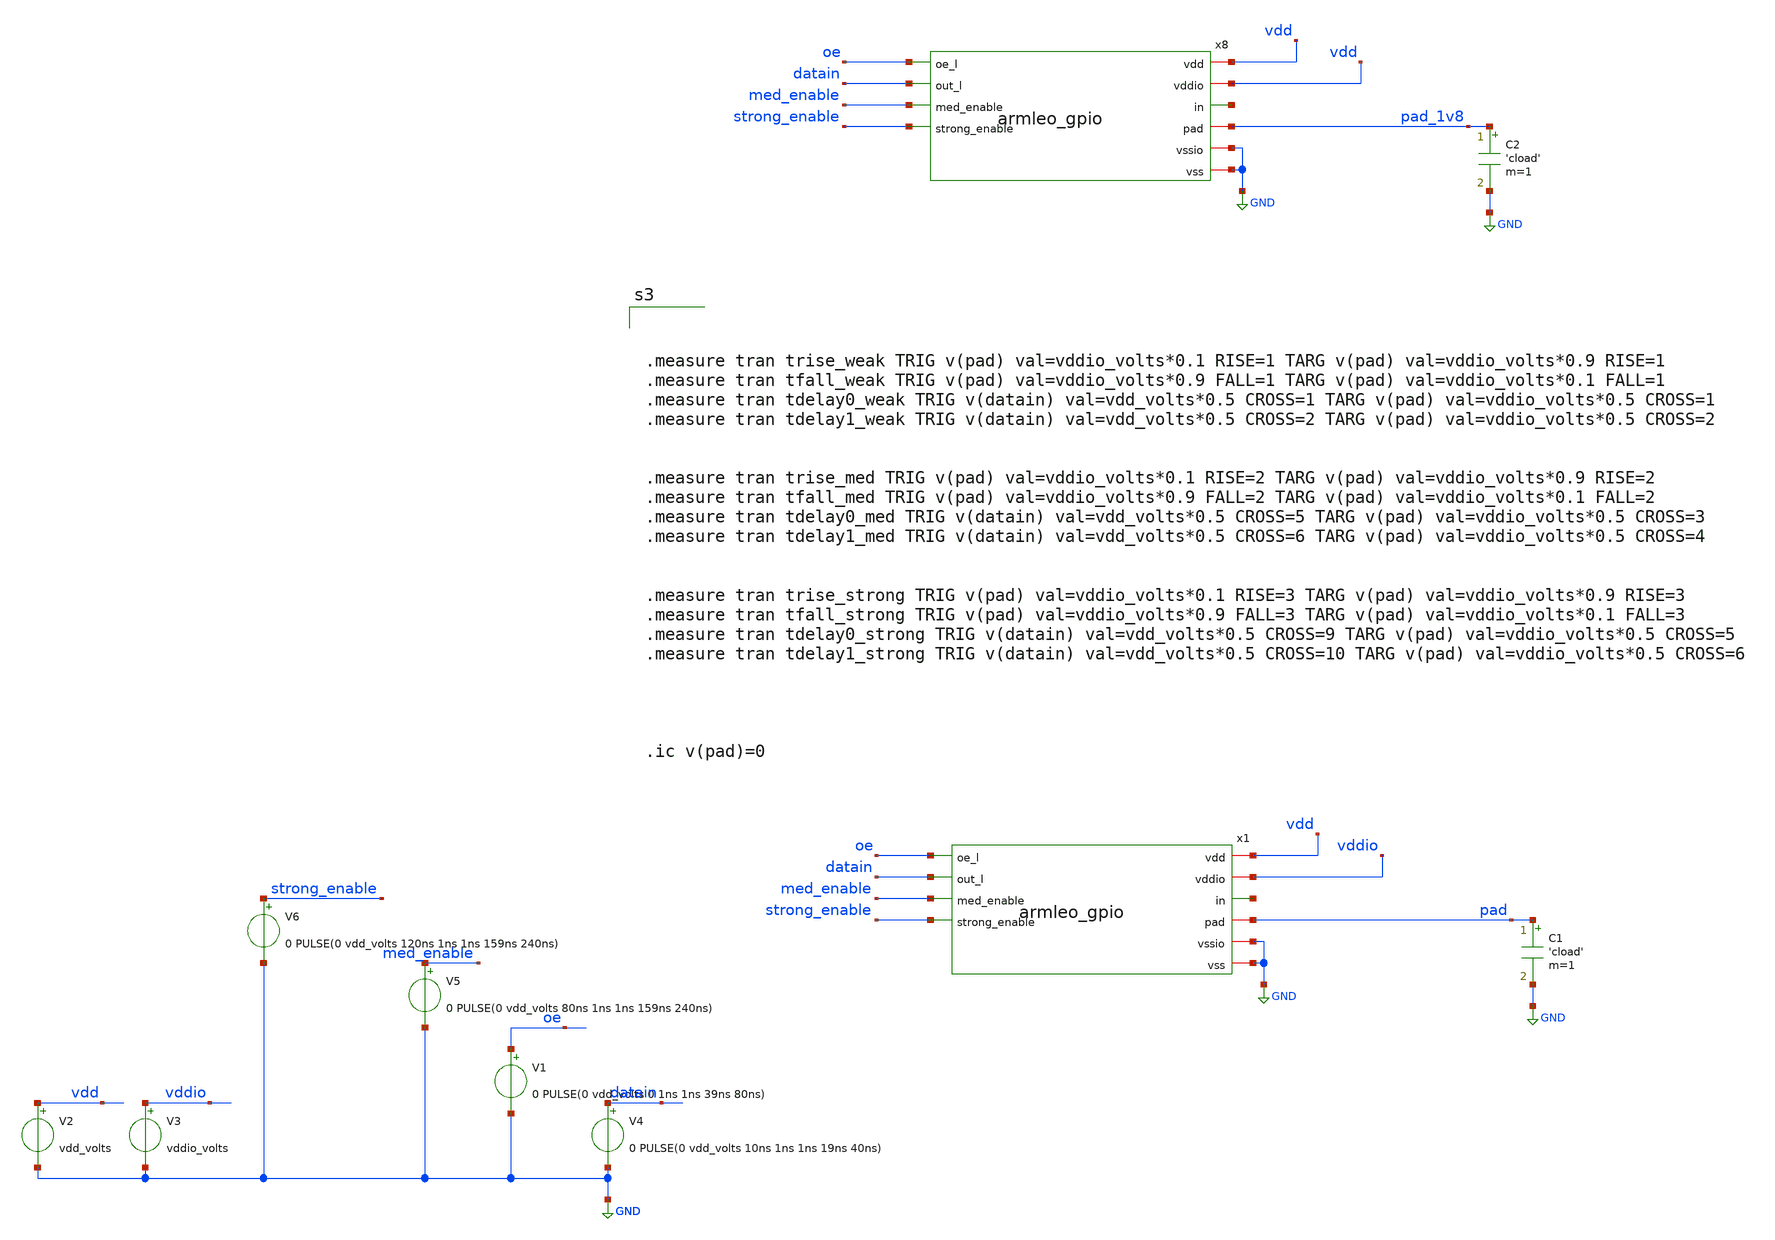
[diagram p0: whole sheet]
** sch_path: xschem/gpio/testbenches/armleo_gpio_worst_tb.sch
**.subckt armleo_gpio_worst_tb
V1 oe GND 0 PULSE(0 vdd_volts 0 1ns 1ns 39ns 80ns)
V2 vdd GND vdd_volts
C1 pad GND 'cload' m=1
V3 vddio GND vddio_volts
x1 vdd vddio net1 pad oe datain med_enable strong_enable GND GND armleo_gpio
V4 datain GND 0 PULSE(0 vdd_volts 10ns 1ns 1ns 19ns 40ns)
x8 vdd vdd net2 pad_1v8 oe datain med_enable strong_enable GND GND armleo_gpio
C2 pad_1v8 GND 'cload' m=1
V5 med_enable GND 0 PULSE(0 vdd_volts 80ns 1ns 1ns 159ns 240ns)
V6 strong_enable GND 0 PULSE(0 vdd_volts 120ns 1ns 1ns 159ns 240ns)
**** begin user architecture code



*.temp -40

*.lib "/opt/pdk_root/sky130A/libs.tech/ngspice/sky130.lib.spice" ff

*.param vdd_volts=1.95
*.param vddio_volts=3.6


.temp 125

.lib "/opt/pdk_root/sky130A/libs.tech/ngspice/sky130.lib.spice" ss

.param vdd_volts=1.65
.param vddio_volts=3.0


.param cload=6pf
*.param cload=12pf


.control
tran 500ps 240ns
write gpio/results/armleo_gpio_tb_6pf_worst.raw

echo "Starting 12pf test"

alterparam cload=12pf
reset
tran 500ps 240ns
write gpio/results/armleo_gpio_tb_12pf_worst.raw


exit
.endc

.param mc_mm_switch=0

*.include "/opt/pdk_root/sky130A/libs.ref/sky130_fd_io/spice/sky130_fd_io.spice"
*.include "/opt/pdk_root/sky130A/libs.ref/sky130_fd_sc_hd/spice/sky130_fd_sc_hd.spice"
*.include "/opt/pdk_root/sky130A/libs.ref/sky130_fd_sc_hvl/spice/sky130_fd_sc_hvl.spice"

.include "libs.spice"






.measure tran trise_weak_1v8 TRIG v(pad_1v8) val=vdd_volts*0.1 RISE=1 TARG v(pad_1v8)
+ val=vdd_volts*0.9 RISE=1
.measure tran tfall_weak_1v8 TRIG v(pad_1v8) val=vdd_volts*0.9 FALL=1 TARG v(pad_1v8)
+ val=vdd_volts*0.1 FALL=1
.measure tran tdelay0_weak_1v8 TRIG v(datain) val=vdd_volts*0.5 CROSS=1 TARG v(pad_1v8)
+ val=vdd_volts*0.5 CROSS=1
.measure tran tdelay1_weak_1v8 TRIG v(datain) val=vdd_volts*0.5 CROSS=2 TARG v(pad_1v8)
+ val=vdd_volts*0.5 CROSS=2

.measure tran trise_med_1v8 TRIG v(pad_1v8) val=vdd_volts*0.1 RISE=2 TARG v(pad_1v8)
+ val=vdd_volts*0.9 RISE=2
.measure tran tfall_med_1v8 TRIG v(pad_1v8) val=vdd_volts*0.9 FALL=2 TARG v(pad_1v8)
+ val=vdd_volts*0.1 FALL=2
.measure tran tdelay0_med_1v8 TRIG v(datain) val=vdd_volts*0.5 CROSS=5 TARG v(pad_1v8)
+ val=vdd_volts*0.5 CROSS=3
.measure tran tdelay1_med_1v8 TRIG v(datain) val=vdd_volts*0.5 CROSS=6 TARG v(pad_1v8)
+ val=vdd_volts*0.5 CROSS=4


.measure tran trise_strong_1v8 TRIG v(pad_1v8) val=vdd_volts*0.1 RISE=3 TARG v(pad_1v8)
+ val=vdd_volts*0.9 RISE=3
.measure tran tfall_strong_1v8 TRIG v(pad_1v8) val=vdd_volts*0.9 FALL=3 TARG v(pad_1v8)
+ val=vdd_volts*0.1 FALL=3
.measure tran tdelay0_strong_1v8 TRIG v(datain) val=vdd_volts*0.5 CROSS=9 TARG v(pad_1v8)
+ val=vdd_volts*0.5 CROSS=5
.measure tran tdelay1_strong_1v8 TRIG v(datain) val=vdd_volts*0.5 CROSS=10 TARG v(pad_1v8)
+ val=vdd_volts*0.5 CROSS=6



.ic v(pad_1v8)=0





.measure tran trise_weak TRIG v(pad) val=vddio_volts*0.1 RISE=1 TARG v(pad) val=vddio_volts*0.9
+ RISE=1
.measure tran tfall_weak TRIG v(pad) val=vddio_volts*0.9 FALL=1 TARG v(pad) val=vddio_volts*0.1
+ FALL=1
.measure tran tdelay0_weak TRIG v(datain) val=vdd_volts*0.5 CROSS=1 TARG v(pad) val=vddio_volts*0.5
+ CROSS=1
.measure tran tdelay1_weak TRIG v(datain) val=vdd_volts*0.5 CROSS=2 TARG v(pad) val=vddio_volts*0.5
+ CROSS=2


.measure tran trise_med TRIG v(pad) val=vddio_volts*0.1 RISE=2 TARG v(pad) val=vddio_volts*0.9
+ RISE=2
.measure tran tfall_med TRIG v(pad) val=vddio_volts*0.9 FALL=2 TARG v(pad) val=vddio_volts*0.1
+ FALL=2
.measure tran tdelay0_med TRIG v(datain) val=vdd_volts*0.5 CROSS=5 TARG v(pad) val=vddio_volts*0.5
+ CROSS=3
.measure tran tdelay1_med TRIG v(datain) val=vdd_volts*0.5 CROSS=6 TARG v(pad) val=vddio_volts*0.5
+ CROSS=4


.measure tran trise_strong TRIG v(pad) val=vddio_volts*0.1 RISE=3 TARG v(pad) val=vddio_volts*0.9
+ RISE=3
.measure tran tfall_strong TRIG v(pad) val=vddio_volts*0.9 FALL=3 TARG v(pad) val=vddio_volts*0.1
+ FALL=3
.measure tran tdelay0_strong TRIG v(datain) val=vdd_volts*0.5 CROSS=9 TARG v(pad)
+ val=vddio_volts*0.5 CROSS=5
.measure tran tdelay1_strong TRIG v(datain) val=vdd_volts*0.5 CROSS=10 TARG v(pad)
+ val=vddio_volts*0.5 CROSS=6




.ic v(pad)=0


**** end user architecture code
**.ends

* expanding   symbol:  gpio/armleo_gpio.sym # of pins=10
** sym_path: xschem/gpio/armleo_gpio.sym
** sch_path: xschem/gpio/armleo_gpio.sch
.subckt armleo_gpio vdd vddio in pad oe_l out_l med_enable strong_enable vssio vss
*.ipin out_l
*.iopin vddio
*.iopin vssio
*.ipin oe_l
*.opin in
*.iopin vdd
*.iopin vss
*.iopin pad
*.ipin med_enable
*.ipin strong_enable
x2 vddio n1 weak_pgate n2 vssio armleo_gpio_lv2hv
x6 esd_pad vss vss vdd vdd in sky130_fd_sc_hvl__buf_16
x37 vddio n3 weak_ngate n4 vssio armleo_gpio_lv2hv
XM1 pad m2_weak_pgate vddio vddio sky130_fd_pr__pfet_g5v0d10v5 L=0.5 W=10 nf=1 ad='int((nf+1)/2) * W/nf * 0.29'
+ as='int((nf+2)/2) * W/nf * 0.29' pd='2*int((nf+1)/2) * (W/nf + 0.29)' ps='2*int((nf+2)/2) * (W/nf + 0.29)'
+ nrd='0.29 / W' nrs='0.29 / W' sa=0 sb=0 sd=0 mult=3*2 m=3*2
XM2 pad m2_weak_ngate vssio vssio sky130_fd_pr__nfet_g5v0d10v5 L=0.5 W=4.5 nf=1 ad='int((nf+1)/2) * W/nf * 0.29'
+ as='int((nf+2)/2) * W/nf * 0.29' pd='2*int((nf+1)/2) * (W/nf + 0.29)' ps='2*int((nf+2)/2) * (W/nf + 0.29)'
+ nrd='0.29 / W' nrs='0.29 / W' sa=0 sb=0 sd=0 mult=3*2 m=3*2
x1 weak_ngate vssio vssio vddio vddio m1_weak_ngate_n sky130_fd_sc_hvl__inv_4
x5 weak_pgate vssio vssio vddio vddio m1_weak_pgate_n sky130_fd_sc_hvl__inv_4
x3 m1_weak_pgate_n vssio vssio vddio vddio m2_weak_pgate sky130_fd_sc_hvl__inv_16
x10 m1_weak_ngate_n vssio vssio vddio vddio m2_weak_ngate sky130_fd_sc_hvl__inv_16
x8 n3 vss vss vdd vdd n4 sky130_fd_sc_hd__inv_4
x12 n1 vss vss vdd vdd n2 sky130_fd_sc_hd__inv_4
x14 oe_l vss vss vdd vdd n5 sky130_fd_sc_hd__inv_4
x16 oe_l out_l vss vss vdd vdd n1 sky130_fd_sc_hd__nand2_4
x17 out_l n5 vss vss vdd vdd n3 sky130_fd_sc_hd__nor2_4
R1 pad esd_pad sky130_fd_pr__res_generic_l1 W=1 L=10 m=1
x4 vddio n1_med med_pgate n2_med vssio armleo_gpio_lv2hv
x7 vddio n3_med med_ngate n4_med vssio armleo_gpio_lv2hv
x9 n3_med vss vss vdd vdd n4_med sky130_fd_sc_hd__inv_4
x11 n1_med vss vss vdd vdd n2_med sky130_fd_sc_hd__inv_4
x13 vddio n1_strong strong_pgate n2_strong vssio armleo_gpio_lv2hv
x15 vddio n3_strong strong_ngate n4_strong vssio armleo_gpio_lv2hv
x18 n3_strong vss vss vdd vdd n4_strong sky130_fd_sc_hd__inv_4
x19 n1_strong vss vss vdd vdd n2_strong sky130_fd_sc_hd__inv_4
XM3 pad m2_med_pgate vddio vddio sky130_fd_pr__pfet_g5v0d10v5 L=0.5 W=10 nf=1 ad='int((nf+1)/2) * W/nf * 0.29'
+ as='int((nf+2)/2) * W/nf * 0.29' pd='2*int((nf+1)/2) * (W/nf + 0.29)' ps='2*int((nf+2)/2) * (W/nf + 0.29)'
+ nrd='0.29 / W' nrs='0.29 / W' sa=0 sb=0 sd=0 mult=3*3 m=3*3
XM4 pad m2_med_ngate vssio vssio sky130_fd_pr__nfet_g5v0d10v5 L=0.5 W=4.5 nf=1 ad='int((nf+1)/2) * W/nf * 0.29'
+ as='int((nf+2)/2) * W/nf * 0.29' pd='2*int((nf+1)/2) * (W/nf + 0.29)' ps='2*int((nf+2)/2) * (W/nf + 0.29)'
+ nrd='0.29 / W' nrs='0.29 / W' sa=0 sb=0 sd=0 mult=3*3 m=3*3
x20 med_ngate vssio vssio vddio vddio m1_med_ngate_n sky130_fd_sc_hvl__inv_4
x21 med_pgate vssio vssio vddio vddio m1_med_pgate_n sky130_fd_sc_hvl__inv_4
x22 m1_med_pgate_n vssio vssio vddio vddio m2_med_pgate sky130_fd_sc_hvl__inv_16
x23 m1_med_ngate_n vssio vssio vddio vddio m2_med_ngate sky130_fd_sc_hvl__inv_16
x24 n6_med vss vss vdd vdd n5_med sky130_fd_sc_hd__inv_4
x25 n5_med out_l vss vss vdd vdd n1_med sky130_fd_sc_hd__nand2_4
x26 out_l n6_med vss vss vdd vdd n3_med sky130_fd_sc_hd__nor2_4
x28 net1 vss vss vdd vdd n5_strong sky130_fd_sc_hd__inv_4
x29 n5_strong out_l vss vss vdd vdd n1_strong sky130_fd_sc_hd__nand2_4
x30 out_l net1 vss vss vdd vdd n3_strong sky130_fd_sc_hd__nor2_4
XM7 pad m2_strong_pgate vddio vddio sky130_fd_pr__pfet_g5v0d10v5 L=0.5 W=10 nf=1 ad='int((nf+1)/2) * W/nf * 0.29'
+ as='int((nf+2)/2) * W/nf * 0.29' pd='2*int((nf+1)/2) * (W/nf + 0.29)' ps='2*int((nf+2)/2) * (W/nf + 0.29)'
+ nrd='0.29 / W' nrs='0.29 / W' sa=0 sb=0 sd=0 mult=3*7 m=3*7
XM8 pad m2_strong_ngate vssio vssio sky130_fd_pr__nfet_g5v0d10v5 L=0.5 W=4.5 nf=1 ad='int((nf+1)/2) * W/nf * 0.29'
+ as='int((nf+2)/2) * W/nf * 0.29' pd='2*int((nf+1)/2) * (W/nf + 0.29)' ps='2*int((nf+2)/2) * (W/nf + 0.29)'
+ nrd='0.29 / W' nrs='0.29 / W' sa=0 sb=0 sd=0 mult=3*7 m=3*7
x36 strong_ngate vssio vssio vddio vddio m1_strong_ngate_n sky130_fd_sc_hvl__inv_4
x38 strong_pgate vssio vssio vddio vddio m1_strong_pgate_n sky130_fd_sc_hvl__inv_4
x39 m1_strong_pgate_n vssio vssio vddio vddio m2_strong_pgate sky130_fd_sc_hvl__inv_16
x40 m1_strong_ngate_n vssio vssio vddio vddio m2_strong_ngate sky130_fd_sc_hvl__inv_16
XM9 pad vssio vssio vssio sky130_fd_pr__esd_nfet_g5v0d10v5 L=0.6 W=5.4 nf=1 ad='int((nf+1)/2) * W/nf * 0.29'
+ as='int((nf+2)/2) * W/nf * 0.29' pd='2*int((nf+1)/2) * (W/nf + 0.29)' ps='2*int((nf+2)/2) * (W/nf + 0.29)'
+ nrd='0.29 / W' nrs='0.29 / W' sa=0 sb=0 sd=0 mult=12 m=12
x27 oe_l med_enable vss vss vdd vdd n6_med sky130_fd_sc_hd__nand2_4
x31 oe_l strong_enable vss vss vdd vdd net1 sky130_fd_sc_hd__nand2_4
.ends


* expanding   symbol:  gpio/armleo_gpio_lv2hv.sym # of pins=5
** sym_path: xschem/gpio/armleo_gpio_lv2hv.sym
** sch_path: xschem/gpio/armleo_gpio_lv2hv.sch
.subckt armleo_gpio_lv2hv VDDH A Y A_N VSSH
*.ipin A
*.iopin VDDH
*.iopin VSSH
*.opin Y
*.ipin A_N
XM2 VSSH A_N Y VSSH sky130_fd_pr__nfet_g5v0d10v5 L=0.5 W=1 nf=1 ad='int((nf+1)/2) * W/nf * 0.29' as='int((nf+2)/2) * W/nf * 0.29'
+ pd='2*int((nf+1)/2) * (W/nf + 0.29)' ps='2*int((nf+2)/2) * (W/nf + 0.29)' nrd='0.29 / W' nrs='0.29 / W'
+ sa=0 sb=0 sd=0 mult=1 m=1
XM5 N1 A VSSH VSSH sky130_fd_pr__nfet_g5v0d10v5 L=0.5 W=1 nf=1 ad='int((nf+1)/2) * W/nf * 0.29' as='int((nf+2)/2) * W/nf * 0.29'
+ pd='2*int((nf+1)/2) * (W/nf + 0.29)' ps='2*int((nf+2)/2) * (W/nf + 0.29)' nrd='0.29 / W' nrs='0.29 / W'
+ sa=0 sb=0 sd=0 mult=1 m=1
XM4 VDDH Y N2 VDDH sky130_fd_pr__pfet_g5v0d10v5 L=0.5 W=1 nf=1 ad='int((nf+1)/2) * W/nf * 0.29' as='int((nf+2)/2) * W/nf * 0.29'
+ pd='2*int((nf+1)/2) * (W/nf + 0.29)' ps='2*int((nf+2)/2) * (W/nf + 0.29)' nrd='0.29 / W' nrs='0.29 / W'
+ sa=0 sb=0 sd=0 mult=1 m=1
XM7 net1 N1 VDDH VDDH sky130_fd_pr__pfet_g5v0d10v5 L=0.5 W=1 nf=1 ad='int((nf+1)/2) * W/nf * 0.29' as='int((nf+2)/2) * W/nf * 0.29'
+ pd='2*int((nf+1)/2) * (W/nf + 0.29)' ps='2*int((nf+2)/2) * (W/nf + 0.29)' nrd='0.29 / W' nrs='0.29 / W'
+ sa=0 sb=0 sd=0 mult=1 m=1
XM9 N1 A N2 VDDH sky130_fd_pr__pfet_g5v0d10v5 L=0.5 W=1 nf=1 ad='int((nf+1)/2) * W/nf * 0.29' as='int((nf+2)/2) * W/nf * 0.29'
+ pd='2*int((nf+1)/2) * (W/nf + 0.29)' ps='2*int((nf+2)/2) * (W/nf + 0.29)' nrd='0.29 / W' nrs='0.29 / W'
+ sa=0 sb=0 sd=0 mult=1 m=1
XM11 net1 A_N Y VDDH sky130_fd_pr__pfet_g5v0d10v5 L=0.5 W=1 nf=1 ad='int((nf+1)/2) * W/nf * 0.29' as='int((nf+2)/2) * W/nf * 0.29'
+ pd='2*int((nf+1)/2) * (W/nf + 0.29)' ps='2*int((nf+2)/2) * (W/nf + 0.29)' nrd='0.29 / W' nrs='0.29 / W'
+ sa=0 sb=0 sd=0 mult=1 m=1
.ends

.GLOBAL GND
.end
